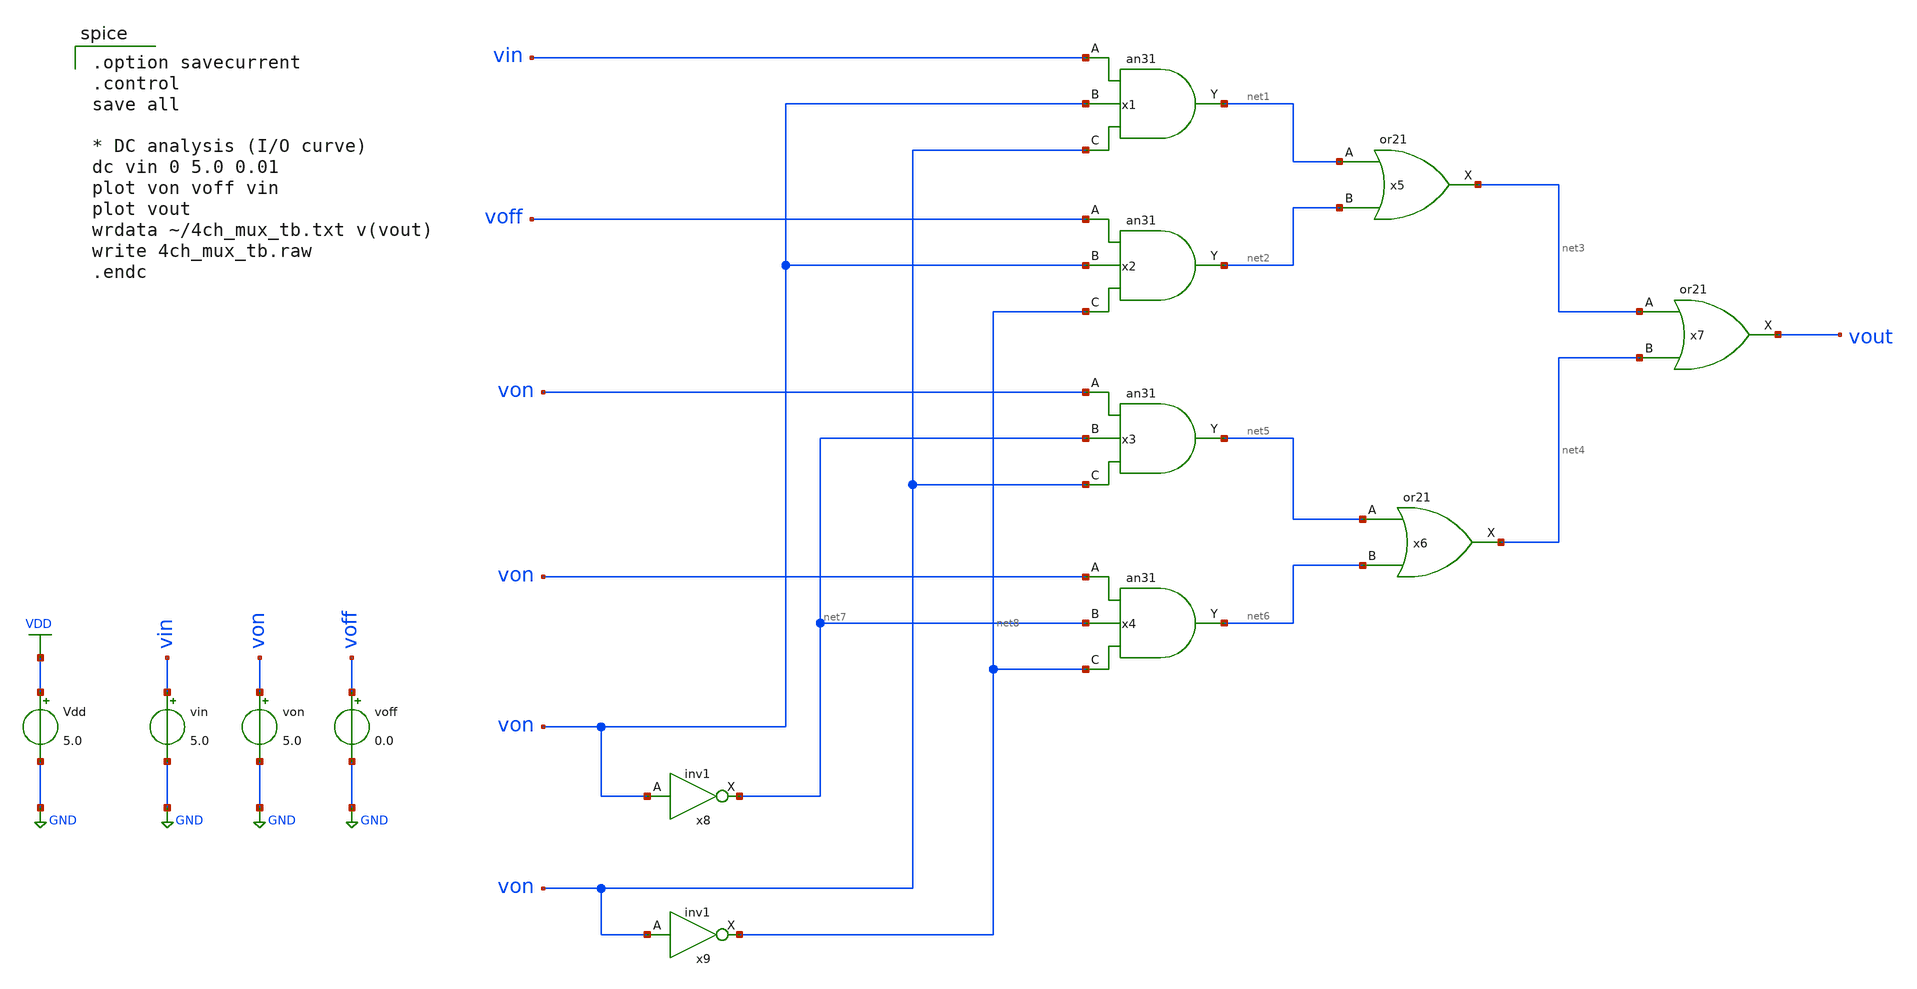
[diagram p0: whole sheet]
** sch_path: member_project/ishi-kai/4ch_mux_tb.sch
**.subckt 4ch_mux_tb
x1 vin von von VDD GND net1 an31
x2 voff von net8 VDD GND net2 an31
x3 von net7 von VDD GND net5 an31
x4 von net7 net8 VDD GND net6 an31
x5 net1 net2 VDD GND net3 or21
x6 net5 net6 VDD GND net4 or21
x7 net3 net4 VDD GND vout or21
x8 von VDD GND net7 inv1
x9 von VDD GND net8 inv1
Vdd VDD GND 5.0
von von GND 5.0
voff voff GND 0.0
vin vin GND 5.0
**** begin user architecture code
 .include $::LIB/mos.lib
.include $::LIB/passive.lib
.include $::LIB/diode.lib

.option savecurrent
.control
save all

* DC analysis (I/O curve)
dc vin 0 5.0 0.01
plot von voff vin
plot vout
wrdata ~/4ch_mux_tb.txt v(vout)
write 4ch_mux_tb.raw
.endc

**** end user architecture code
**.ends
.GLOBAL VDD
.GLOBAL GND
.end
